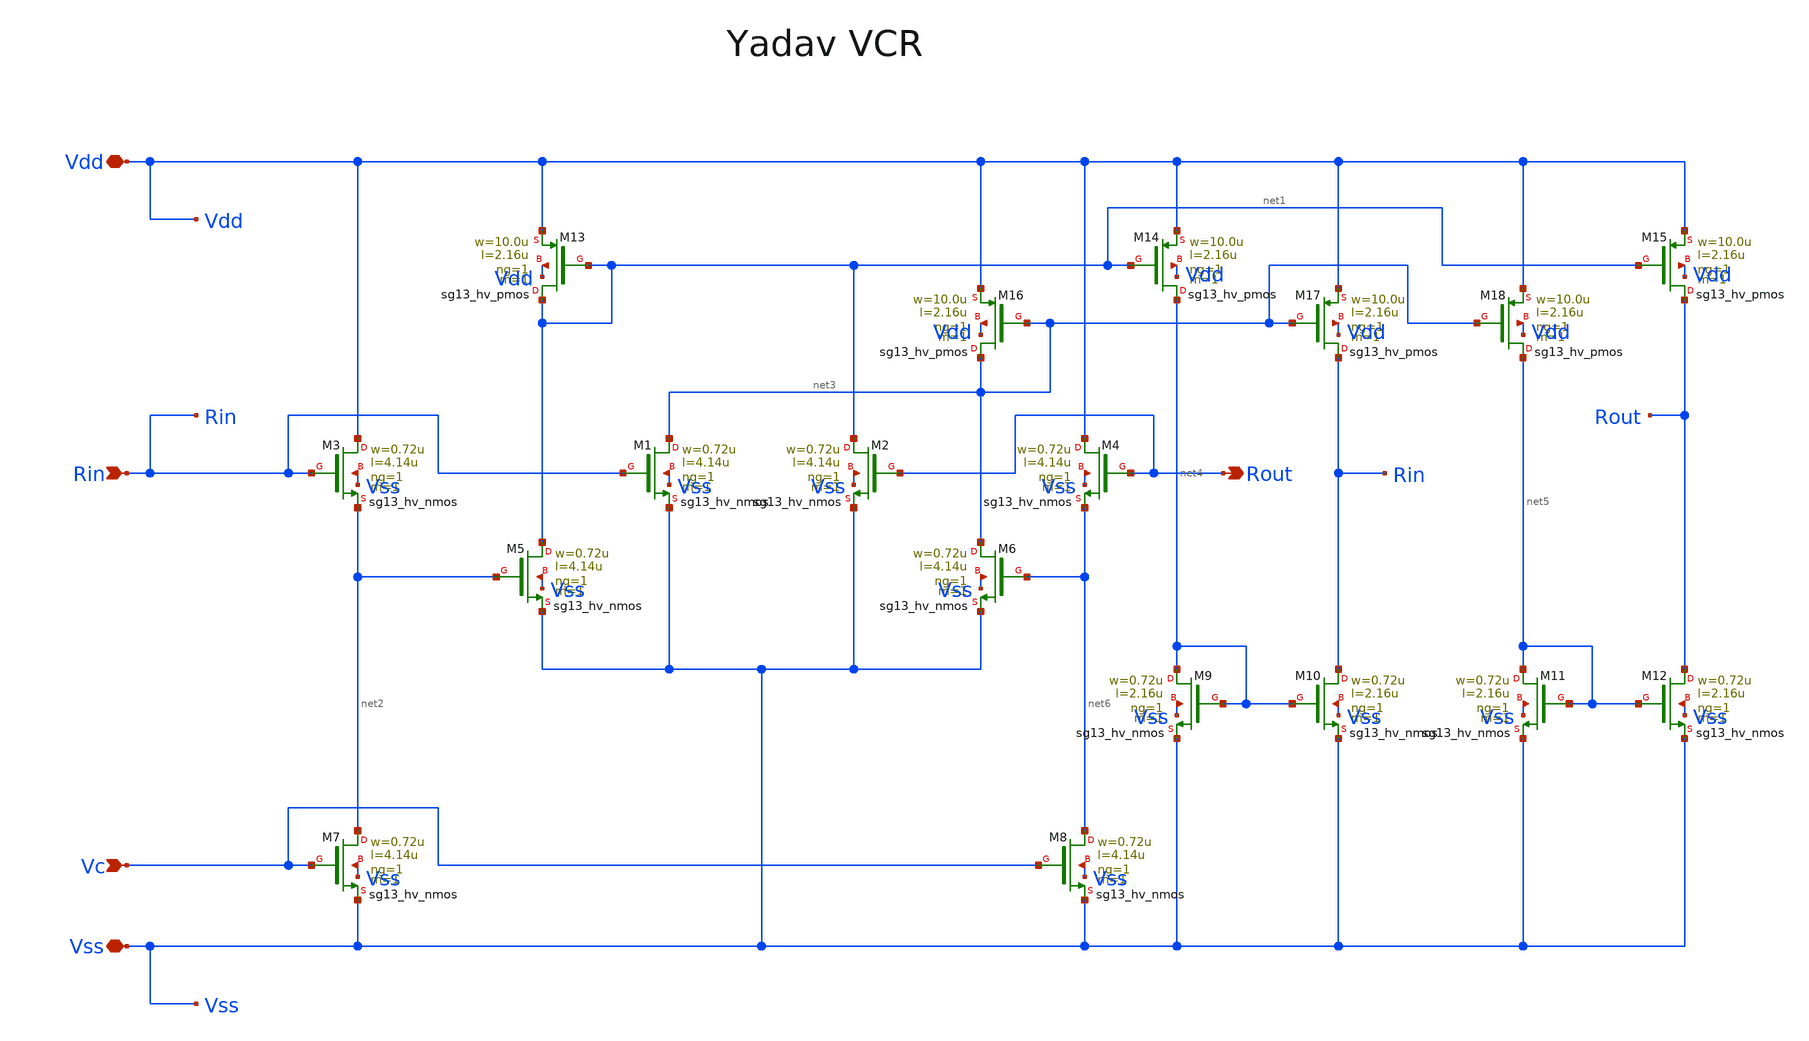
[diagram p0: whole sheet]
** sch_path: macros/heichips26_analog_project/macros/yadav/schematic/xschem/YadavVCR.sch
**.subckt YadavVCR Vc Vss Vdd Rin Rout
*.ipin Vc
*.iopin Vss
*.iopin Vdd
*.ipin Rin
*.opin Rout
XM3 Vdd Rin net2 Vss sg13_hv_nmos w=0.72u l=4.14u ng=1 m=1 mm_ok=1
XM13 net1 net1 Vdd Vdd sg13_hv_pmos w=10.0u l=2.16u ng=1 m=1 mm_ok=1
XM1 net3 Rin Vss Vss sg13_hv_nmos w=0.72u l=4.14u ng=1 m=1 mm_ok=1
XM5 net1 net2 Vss Vss sg13_hv_nmos w=0.72u l=4.14u ng=1 m=1 mm_ok=1
XM2 net1 Rout Vss Vss sg13_hv_nmos w=0.72u l=4.14u ng=1 m=1 mm_ok=1
XM16 net3 net3 Vdd Vdd sg13_hv_pmos w=10.0u l=2.16u ng=1 m=1 mm_ok=1
XM7 net2 Vc Vss Vss sg13_hv_nmos w=0.72u l=4.14u ng=1 m=1 mm_ok=1
XM6 net3 net6 Vss Vss sg13_hv_nmos w=0.72u l=4.14u ng=1 m=1 mm_ok=1
XM14 net4 net1 Vdd Vdd sg13_hv_pmos w=10.0u l=2.16u ng=1 m=1 mm_ok=1
XM8 net6 Vc Vss Vss sg13_hv_nmos w=0.72u l=4.14u ng=1 m=1 mm_ok=1
XM4 Vdd Rout net6 Vss sg13_hv_nmos w=0.72u l=4.14u ng=1 m=1 mm_ok=1
XM9 net4 net4 Vss Vss sg13_hv_nmos w=0.72u l=2.16u ng=1 m=1 mm_ok=1
XM10 Rin net4 Vss Vss sg13_hv_nmos w=0.72u l=2.16u ng=1 m=1 mm_ok=1
XM17 Rin net3 Vdd Vdd sg13_hv_pmos w=10.0u l=2.16u ng=1 m=1 mm_ok=1
XM18 net5 net3 Vdd Vdd sg13_hv_pmos w=10.0u l=2.16u ng=1 m=1 mm_ok=1
XM11 net5 net5 Vss Vss sg13_hv_nmos w=0.72u l=2.16u ng=1 m=1 mm_ok=1
XM12 Rout net5 Vss Vss sg13_hv_nmos w=0.72u l=2.16u ng=1 m=1 mm_ok=1
XM15 Rout net1 Vdd Vdd sg13_hv_pmos w=10.0u l=2.16u ng=1 m=1 mm_ok=1
**.ends
.end
